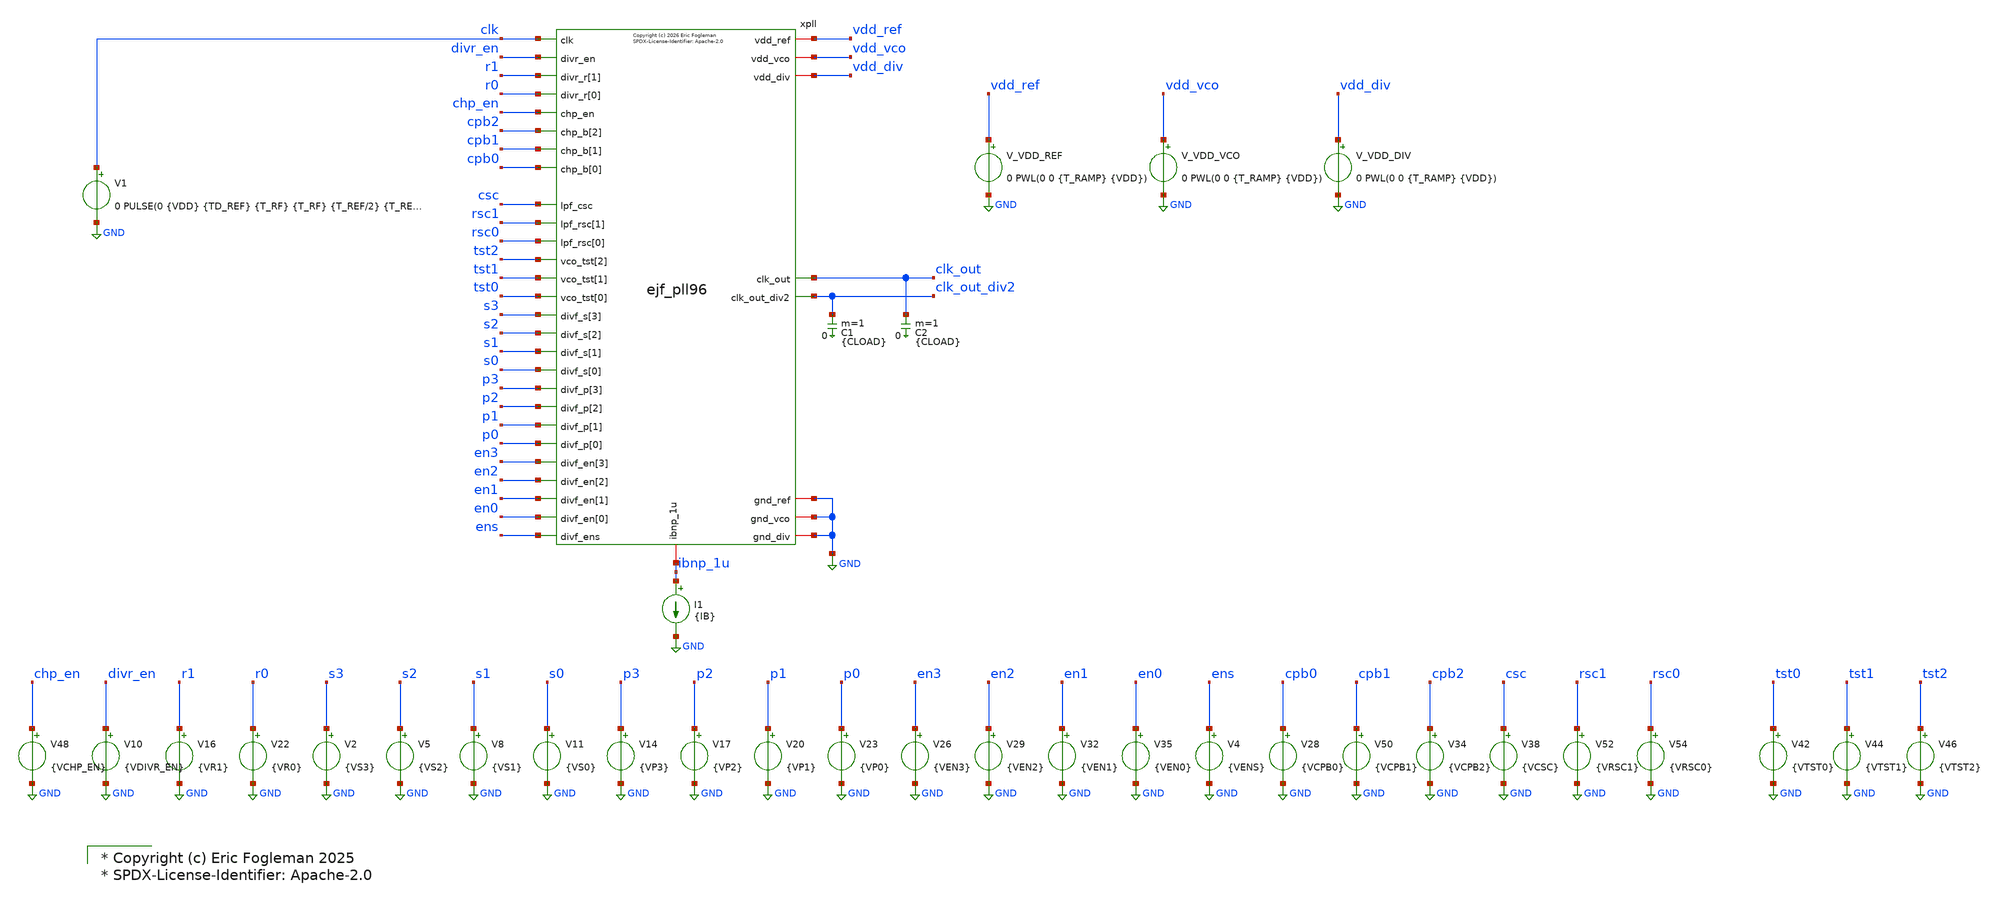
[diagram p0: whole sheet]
** sch_path: xschem/tb_ejf_pll96_top_reg.sch

* Copyright (c) Eric Fogleman 2025
* SPDX-License-Identifier: Apache-2.0

**.subckt tb_ejf_pll96_top_reg
V_VDD_REF vdd_ref GND 0 PWL(0 0 {T_RAMP} {VDD})
.save i(v_vdd_ref)
V1 clk GND 0 PULSE(0 {VDD} {TD_REF} {T_RF} {T_RF} {T_REF/2} {T_REF})
xpll vdd_vco vdd_div vdd_ref clk_out r1 clk_out_div2 r0 clk divr_en GND s3 s2 s1 s0 p3 GND p2 cpb2
+ p1 tst2 ibnp_1u cpb1 p0 tst1 cpb0 tst0 en3 en2 chp_en en1 csc en0 rsc1 ens rsc0 GND ejf_pll96
V_VDD_VCO vdd_vco GND 0 PWL(0 0 {T_RAMP} {VDD})
.save i(v_vdd_vco)
V_VDD_DIV vdd_div GND 0 PWL(0 0 {T_RAMP} {VDD})
.save i(v_vdd_div)
V2 s3 GND {VS3}
V5 s2 GND {VS2}
V8 s1 GND {VS1}
V11 s0 GND {VS0}
V14 p3 GND {VP3}
V17 p2 GND {VP2}
V20 p1 GND {VP1}
V23 p0 GND {VP0}
V26 en3 GND {VEN3}
V29 en2 GND {VEN2}
V32 en1 GND {VEN1}
V35 en0 GND {VEN0}
V4 ens GND {VENS}
I1 ibnp_1u GND {IB}
V10 divr_en GND {VDIVR_EN}
V16 r1 GND {VR1}
V22 r0 GND {VR0}
V28 cpb0 GND {VCPB0}
V34 cpb2 GND {VCPB2}
V38 csc GND {VCSC}
C1 clk_out_div2 0 {CLOAD} m=1
C2 clk_out 0 {CLOAD} m=1
V42 tst0 GND {VTST0}
V44 tst1 GND {VTST1}
V46 tst2 GND {VTST2}
V48 chp_en GND {VCHP_EN}
V50 cpb1 GND {VCPB1}
V52 rsc1 GND {VRSC1}
V54 rsc0 GND {VRSC0}
**** begin user architecture code

* ejf_pfd test
.lib ~/.ciel/sky130A/libs.tech/combined/sky130.lib.spice tt
.include ~/.ciel/sky130A/libs.ref/sky130_fd_sc_ls/spice/sky130_fd_sc_ls.spice
*** ejf_pll96 regression
*** run with:
*** ngspice -b -r top_reg.raw -o top_reg.out tb_ejf_pll96_top_reg.spice

*** simulation setup
.option temp=27
.param VDD=1.8
.param TD_REF=50n
.param T_RF=300p
.param T_RAMP=50n
.param CP=10f
.param CLOAD=100f
.param IB=1u
.param VDIVR_EN=1.8
.param VCHP_EN=1.8
.param VTST0=0
.param VTST1=0
.param VTST2=0

*** mode-dependent options
.include config.inc



* Run transient
* default reltol=1e-3 vntol=1e-6 abstol=1e-12
.options  reltol=1e-4 vntol=1e-7 abstol=1e-13
*.options klu
.control
   save i(v_vdd_ref) i(v_vdd_vco) i(v_vdd_div)
   save clk clk_out clk_out_div2 ibnp_1u
   save xpll.qref xpll.qref_b xpll.qclk xpll.qclk_b xpll.vc xpll.vco_outp xpll.vco_outn
   save xpll.xvco.vhi xpll.clk_divf xpll.clk_ref
   save xpll.xvco.x0p xpll.xvco.x0n xpll.xvco.x1p xpll.xvco.x1n xpll.xvco.x2p xpll.xvco.x2n
+ xpll.xvco.x3p xpll.xvco.x3n
   save xpll.xchp.cp_repl xpll.xchp.mp1g xpll.xchp.mp1cg xpll.xchp.mn1g xpll.xchp.mn1cg
+ xpll.xchp.amp_inp
   save xpll.xchp.mn1d xpll.xchp.mp1d xpll.xchp.mp1cd xpll.xchp.mn1cd
   save xpll.xlpf.mpc2g xpll.xlpf.bp
   tran 1n 20u
   write tb_ejf_pll96_top_reg.raw
   meas tran idd_ref avg i(v_vdd_ref) from=18u to=20u
   meas tran idd_vco avg i(v_vdd_vco) from=18u to=20u
   meas tran idd_div avg i(v_vdd_div) from=18u to=20u
   meas tran T_CLK_OUT trig v(clk_out) val=0.9 rise=1 td=19u targ v(clk_out) val=0.9 rise=2 td=19u
   print 1/T_CLK_OUT
.endc


**** end user architecture code
**.ends
.GLOBAL GND
.end
